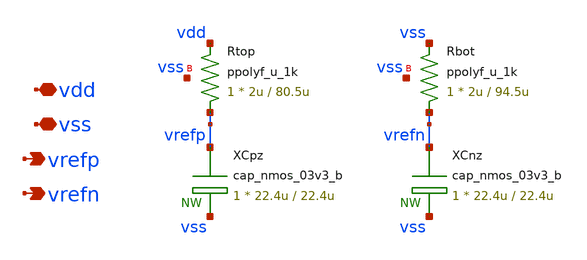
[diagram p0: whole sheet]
** sch_path: blocks/adc/comp-array/refgen.sch
**.subckt refgen vdd vss vrefp vrefn
*.iopin vdd
*.iopin vss
*.opin vrefp
*.opin vrefn
XRtop vrefp vdd vss ppolyf_u_1k r_width=2u r_length=80.5u m=1
XRbot vrefn vss vss ppolyf_u_1k r_width=2u r_length=94.5u m=1
XCpz vrefp vss cap_nmos_03v3_b c_width=22.4u c_length=22.4u m=1
XCnz vrefn vss cap_nmos_03v3_b c_width=22.4u c_length=22.4u m=1
**.ends
.end
